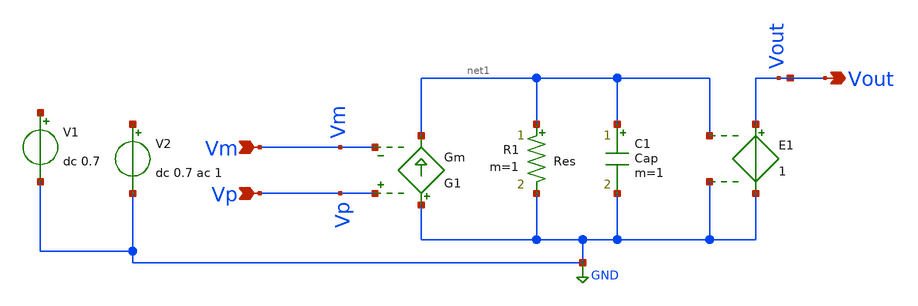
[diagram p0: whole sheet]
** sch_path: EE_628_LDO/Ideal_Error_amp.sch
* Copyright 2023 IHP PDK Authors
**.subckt Ideal_Error_amp Vm Vp Vout
*.ipin Vm
*.ipin Vp
*.opin Vout
E1 Vout GND net1 GND 1
G1 GND net1 Vp Vm Gm
R1 net1 GND Res m=1
C1 net1 GND Cap m=1
V2 net2 GND dc 0.7 ac 1
V1 net3 GND dc 0.7
**** begin user architecture code

.lib /foss/pdks/sg13g2/libs.tech/ngspice/models/cornerMOSlv.lib mos_tt
.lib /foss/pdks/sg13g2/libs.tech/ngspice/models/cornerRES.lib res_typ
**.lib /foss/pdks/sg13g2/libs.tech/ngspice/models/sg13g2_moslv_mod.lib mos_tt
**.lib /foss/pdks/sg13g2/libs.tech/ngspice/models/sg13g2_moslv_parm.lib mos_tt
**.lib /foss/pdks/sg13g2/libs.tech/ngspice/models/sg13g2_moslv_stat.lib mos_tt

**** end user architecture code
**.ends
.GLOBAL GND
.end
